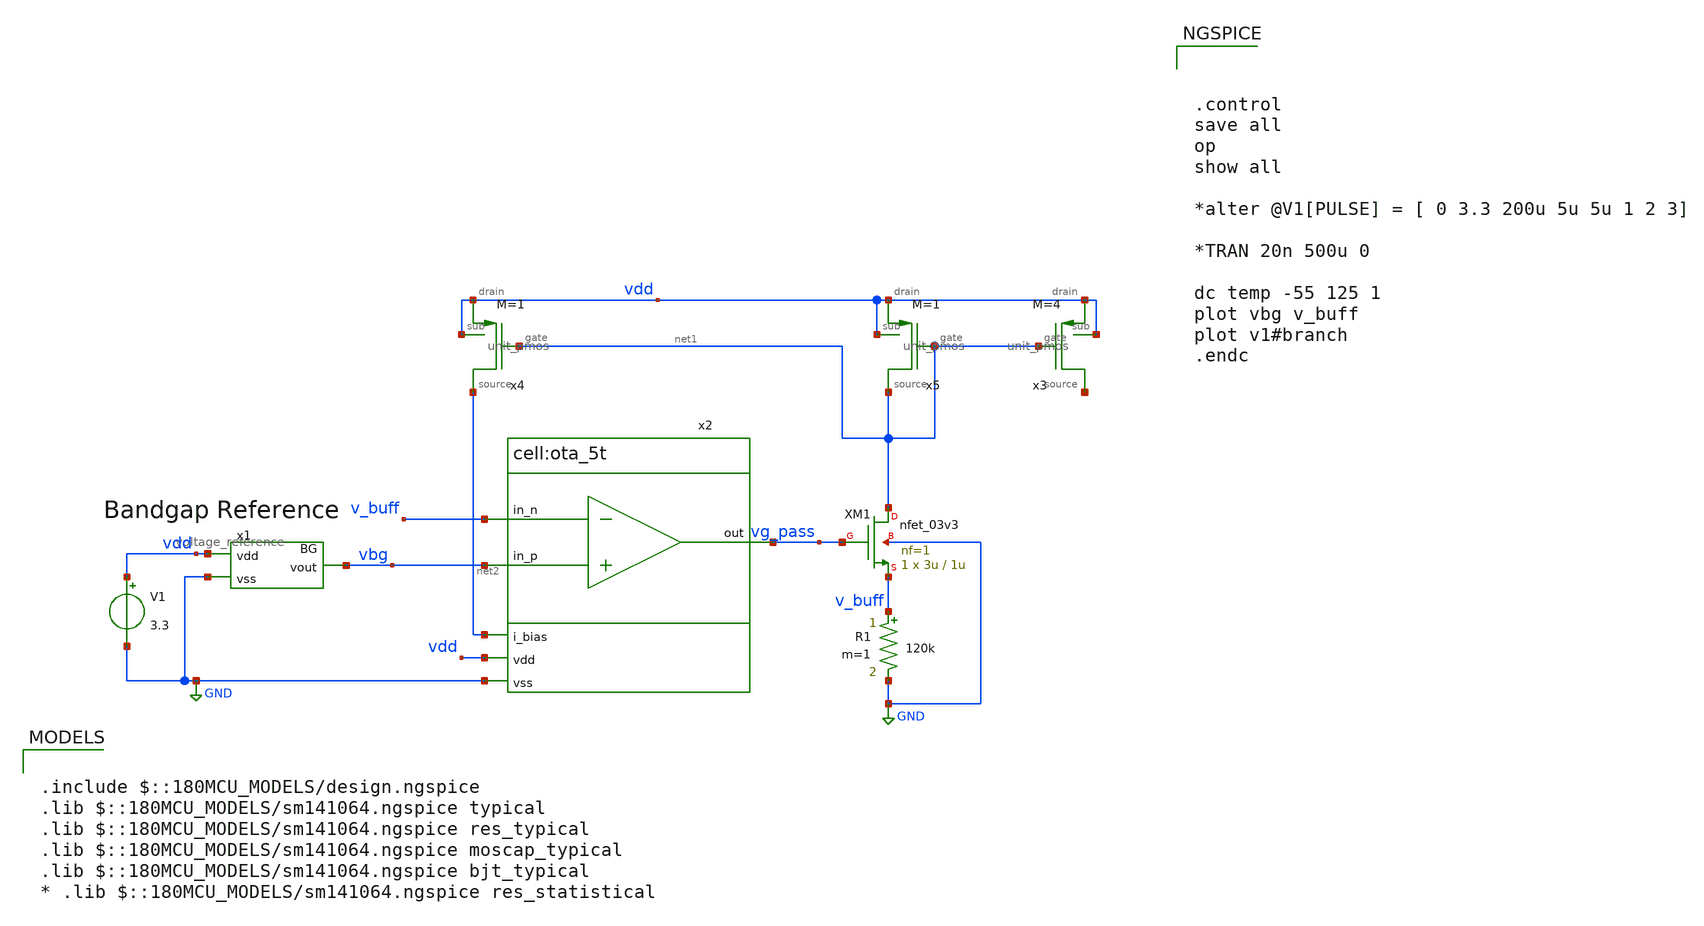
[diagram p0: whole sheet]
** sch_path: designs/switch_matrix_gf180mcu_9t5v0-main/designs/libs/tb_analog/vref/vref_tb.sch
**.subckt vref_tb
V1 vdd GND 3.3
x1 vdd vbg GND voltage_reference
x3 vdd vdd net1 net3 unit_pmos M=4
R1 v_buff GND 120k m=1
x4 vdd vdd net1 net2 unit_pmos M=1
x2 vdd vg_pass vbg v_buff net2 GND ota_5t
XM1 net1 vg_pass v_buff GND nfet_03v3 L=1u W=3u nf=1 ad='int((nf+1)/2) * W/nf * 0.18u' as='int((nf+2)/2) * W/nf * 0.18u'
+ pd='2*int((nf+1)/2) * (W/nf + 0.18u)' ps='2*int((nf+2)/2) * (W/nf + 0.18u)' nrd='0.18u / W' nrs='0.18u / W'
+ sa=0 sb=0 sd=0 m=1
x5 vdd vdd net1 net1 unit_pmos M=1
**** begin user architecture code



.control
save all
op
show all

*alter @V1[PULSE] = [ 0 3.3 200u 5u 5u 1 2 3]

*TRAN 20n 500u 0

dc temp -55 125 1
plot vbg v_buff
plot v1#branch
.endc



.include $::180MCU_MODELS/design.ngspice
.lib $::180MCU_MODELS/sm141064.ngspice typical
.lib $::180MCU_MODELS/sm141064.ngspice res_typical
.lib $::180MCU_MODELS/sm141064.ngspice moscap_typical
.lib $::180MCU_MODELS/sm141064.ngspice bjt_typical
* .lib $::180MCU_MODELS/sm141064.ngspice res_statistical

**** end user architecture code
**.ends
.GLOBAL GND
.end
